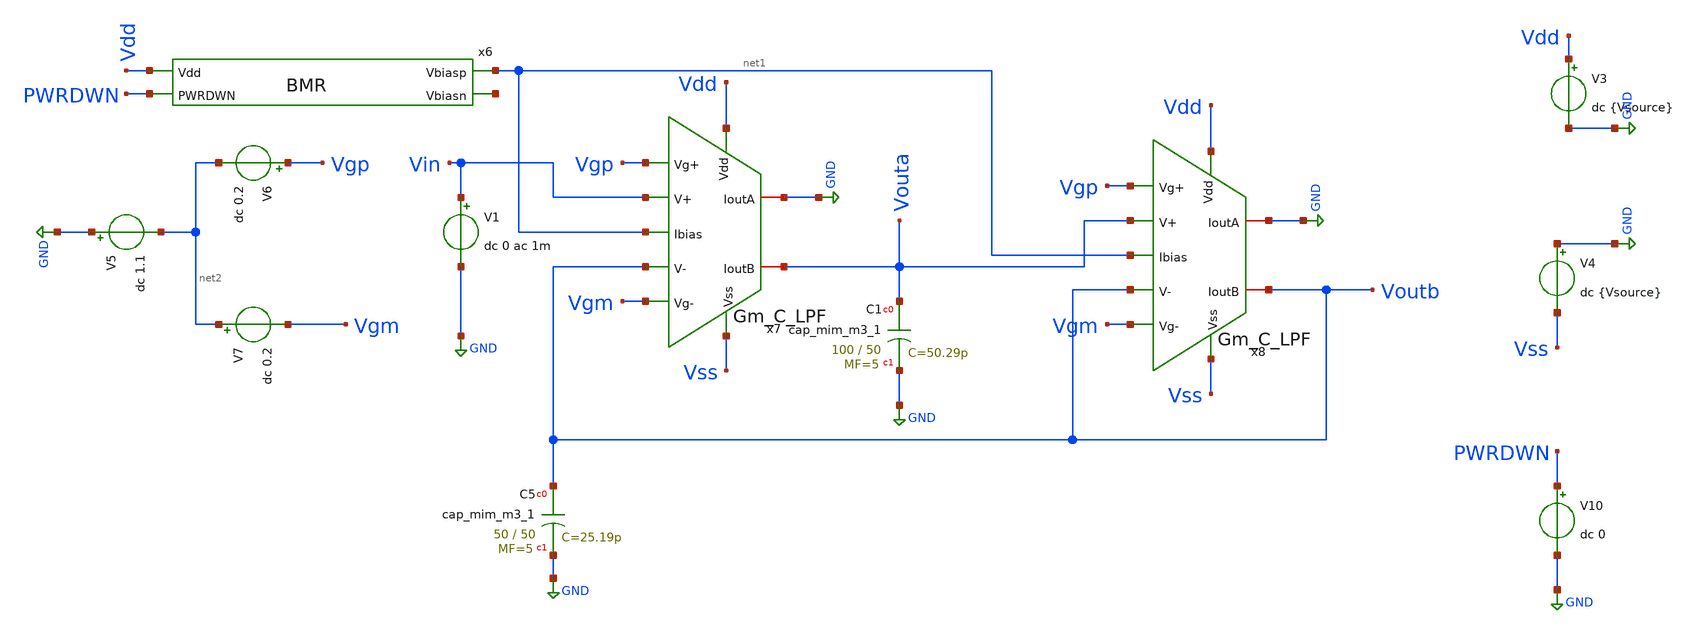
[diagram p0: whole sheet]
** sch_path: xschem/GmC_TB.sch
**.subckt GmC_TB
V4 GND Vss dc {Vsource}
V3 Vdd GND dc {Vsource}
V10 PWRDWN GND dc 0
V1 Vin GND dc 0 ac 1m
V5 GND net2 dc 1.1
V6 Vgp net2 dc 0.2
x6 Vdd net1 net3 PWRDWN BMR
x7 Vdd Vss Vgp Vgm GND Vouta Vin Voutb net1 Gm_C_LPF
V7 net2 Vgm dc 0.2
x8 Vdd Vss Vgp Vgm GND Voutb Vouta Voutb net1 Gm_C_LPF
XC5 Voutb GND sky130_fd_pr__cap_mim_m3_1 W=50 L=50 MF=5 m=5
XC1 Vouta GND sky130_fd_pr__cap_mim_m3_1 W=100 L=50 MF=5 m=5
**** begin user architecture code


.lib /foss/pdks/sky130A/libs.tech/combined/sky130.lib.spice ss_mm

***Centered at 40C and varies to a range of -20 to 100; with 20C being 1-standard dev***
.param TEMPGAUSS = agauss(40, 60, 3)

***Centered at 2.5V and varies to a range of 2V to 3V; with 0.16mV being 1-standard dev***
.param VOLTGAUSS = agauss(2.5, 0.5, 3)

.param ptemp = 'TEMPGAUSS'

.param Vsource = 'VOLTGAUSS'
.options temp = {ptemp}

.csparam ctemp = {ptemp}
.csparam cvolt = {Vsource}


.control
 let T = 27
 let V = 2.5

 let i_count = 100
 let T_vec = vector(i_count)
 let V_vec = vector(i_count)

 let CUTOFF_vec = vector(i_count)

 let index = 0

 set wr_vecnames
 dowhile index <= 100
   save all
   *tran 1u 2m
   *dc V1 -10m 10m 1m
   ac dec 100 0.1 1MEG

   write GMC_LPF_CUTOFFS_SS_MM_PVT.raw

   set noprintscale

   let gaindb = 'db(voutb/vin)'
   meas ac maxgain MAX gaindb
   let cutoffdb = 'maxgain - 3'
   meas ac cutoff_freq WHEN gaindb = cutoffdb
   let CUTOFF_vec[index] = 'cutoff_freq'

   **OFFSET**

   ***meas dc Off FIND v(voutb) WHEN v(vin) = 0 RISE = 1

   ***let OFFSET_vec[index] = 'Off'

   set appendwrite


   let V = $&cvolt
   let T = $&ctemp

   echo -n This is $&V
   echo -n This is $&T
   echo -n This is $&index

   let V_vec[index] = 'V'
   let T_vec[index] = 'T'

   let index = index + 1
   reset
 end
  **OL AC
  *** print col GAIN_vec UGW_vec PM_vec T_vec V_vec > FDA_AC_CM_GAIN_UGW_PM_SS_PVT.txt
  **Offset
   ***print col OFFSET_vec T_vec V_vec > GMC_LPF_OFFSETS_SS_MM_PVT.txt
    print col CUTOFF_vec T_vec V_vec > GMC_AC_CUTOFF_SS_MM_PVT.txt

.endc
.end

**** end user architecture code
**.ends

* expanding   symbol:  BMR.sym # of pins=4
** sym_path: xschem/BMR.sym
** sch_path: xschem/BMR.sch
.subckt BMR Vdd Vbiasp Vbiasn PWRDWN
*.ipin Vdd
*.opin Vbiasn
*.opin Vbiasp
*.ipin PWRDWN
XM3 Vbiasn Vbiasn GND GND sky130_fd_pr__nfet_g5v0d10v5 L=3 W=1.4 nf=1 ad='int((1 + 1)/2) * 1.4 / 1 * 0.29'
+ as='int((1 + 2)/2) * 1.4 / 1 * 0.29' pd='2*int((1 + 1)/2) * (1.4 / 1 + 0.29)' ps='2*int((1 + 2)/2) * (1.4 / 1 + 0.29)'
+ nrd='0.29 / 1.4 ' nrs='0.29 / 1.4 ' sa=0 sb=0 sd=0 mult=1 m=1
XM1 Vbiasp Vbiasp Vdd Vdd sky130_fd_pr__pfet_g5v0d10v5 L=3 W=31 nf=8 ad='int((8 + 1)/2) * 31 / 8 * 0.29'
+ as='int((8 + 2)/2) * 31 / 8 * 0.29' pd='2*int((8 + 1)/2) * (31 / 8 + 0.29)' ps='2*int((8 + 2)/2) * (31 / 8 + 0.29)'
+ nrd='0.29 / 31 ' nrs='0.29 / 31 ' sa=0 sb=0 sd=0 mult=2 m=2
XM2 Vbiasn Vbiasp Vdd Vdd sky130_fd_pr__pfet_g5v0d10v5 L=3 W=31 nf=8 ad='int((8 + 1)/2) * 31 / 8 * 0.29'
+ as='int((8 + 2)/2) * 31 / 8 * 0.29' pd='2*int((8 + 1)/2) * (31 / 8 + 0.29)' ps='2*int((8 + 2)/2) * (31 / 8 + 0.29)'
+ nrd='0.29 / 31 ' nrs='0.29 / 31 ' sa=0 sb=0 sd=0 mult=2 m=2
XM11 net1 PWRUP Vdd Vdd sky130_fd_pr__pfet_g5v0d10v5 L=10 W=1 nf=1 ad='int((1 + 1)/2) * 1 / 1 * 0.29'
+ as='int((1 + 2)/2) * 1 / 1 * 0.29' pd='2*int((1 + 1)/2) * (1 / 1 + 0.29)' ps='2*int((1 + 2)/2) * (1 / 1 + 0.29)'
+ nrd='0.29 / 1 ' nrs='0.29 / 1 ' sa=0 sb=0 sd=0 mult=1 m=1
XM4 Vbiasp Vbiasn net2 GND sky130_fd_pr__nfet_g5v0d10v5 L=3 W=1.4 nf=1 ad='int((1 + 1)/2) * 1.4 / 1 * 0.29'
+ as='int((1 + 2)/2) * 1.4 / 1 * 0.29' pd='2*int((1 + 1)/2) * (1.4 / 1 + 0.29)' ps='2*int((1 + 2)/2) * (1.4 / 1 + 0.29)'
+ nrd='0.29 / 1.4 ' nrs='0.29 / 1.4 ' sa=0 sb=0 sd=0 mult=2 m=2
XM5 net1 Vbiasn GND GND sky130_fd_pr__nfet_g5v0d10v5 L=3 W=1.4 nf=1 ad='int((1 + 1)/2) * 1.4 / 1 * 0.29'
+ as='int((1 + 2)/2) * 1.4 / 1 * 0.29' pd='2*int((1 + 1)/2) * (1.4 / 1 + 0.29)' ps='2*int((1 + 2)/2) * (1.4 / 1 + 0.29)'
+ nrd='0.29 / 1.4 ' nrs='0.29 / 1.4 ' sa=0 sb=0 sd=0 mult=1 m=1
XM7 net3 net1 Vbiasn GND sky130_fd_pr__nfet_g5v0d10v5 L=1 W=20 nf=1 ad='int((1 + 1)/2) * 20 / 1 * 0.29'
+ as='int((1 + 2)/2) * 20 / 1 * 0.29' pd='2*int((1 + 1)/2) * (20 / 1 + 0.29)' ps='2*int((1 + 2)/2) * (20 / 1 + 0.29)'
+ nrd='0.29 / 20 ' nrs='0.29 / 20 ' sa=0 sb=0 sd=0 mult=1 m=1
x1 Vdd PWRUP PWRDWN GND NOT_GATE
XM12 Vbiasp PWRUP net3 GND sky130_fd_pr__nfet_g5v0d10v5 L=1 W=20 nf=1 ad='int((1 + 1)/2) * 20 / 1 * 0.29'
+ as='int((1 + 2)/2) * 20 / 1 * 0.29' pd='2*int((1 + 1)/2) * (20 / 1 + 0.29)' ps='2*int((1 + 2)/2) * (20 / 1 + 0.29)'
+ nrd='0.29 / 20 ' nrs='0.29 / 20 ' sa=0 sb=0 sd=0 mult=1 m=1
XM9 Vbiasp PWRUP Vdd Vdd sky130_fd_pr__pfet_g5v0d10v5 L=1 W=3 nf=1 ad='int((1 + 1)/2) * 3 / 1 * 0.29'
+ as='int((1 + 2)/2) * 3 / 1 * 0.29' pd='2*int((1 + 1)/2) * (3 / 1 + 0.29)' ps='2*int((1 + 2)/2) * (3 / 1 + 0.29)'
+ nrd='0.29 / 3 ' nrs='0.29 / 3 ' sa=0 sb=0 sd=0 mult=1 m=1
XM10 Vbiasn PWRDWN GND GND sky130_fd_pr__nfet_g5v0d10v5 L=1 W=1 nf=1 ad='int((1 + 1)/2) * 1 / 1 * 0.29'
+ as='int((1 + 2)/2) * 1 / 1 * 0.29' pd='2*int((1 + 1)/2) * (1 / 1 + 0.29)' ps='2*int((1 + 2)/2) * (1 / 1 + 0.29)'
+ nrd='0.29 / 1 ' nrs='0.29 / 1 ' sa=0 sb=0 sd=0 mult=1 m=1
XR5 GND net2 GND sky130_fd_pr__res_xhigh_po_2p85 L=71.25 mult=1 m=1
XC10 Vdd net1 sky130_fd_pr__cap_mim_m3_1 W=10 L=10 MF=5 m=5
XC2 Vdd Vbiasp sky130_fd_pr__cap_mim_m3_1 W=10 L=10 MF=5 m=5
XC1 Vbiasn GND sky130_fd_pr__cap_mim_m3_1 W=10 L=10 MF=5 m=5
.ends


* expanding   symbol:  Gm_C_LPF.sym # of pins=9
** sym_path: xschem/Gm_C_LPF.sym
** sch_path: xschem/Gm_C_LPF.sch
.subckt Gm_C_LPF Vdd Vss Vg+ Vg- IoutA IoutB V+ V- Ibias
*.ipin V-
*.ipin V+
*.ipin Vdd
*.ipin Vss
*.ipin Ibias
*.ipin Vg-
*.ipin Vg+
*.iopin IoutA
*.iopin IoutB
XM1 net2 Ibias Vdd Vdd sky130_fd_pr__pfet_g5v0d10v5 L=3 W=31 nf=8 ad='int((8 + 1)/2) * 31 / 8 * 0.29'
+ as='int((8 + 2)/2) * 31 / 8 * 0.29' pd='2*int((8 + 1)/2) * (31 / 8 + 0.29)' ps='2*int((8 + 2)/2) * (31 / 8 + 0.29)'
+ nrd='0.29 / 31 ' nrs='0.29 / 31 ' sa=0 sb=0 sd=0 mult=1 m=1
XM2 net3 V- net2 Vdd sky130_fd_pr__pfet_g5v0d10v5 L=3 W=40 nf=4 ad='int((4 + 1)/2) * 40 / 4 * 0.29' as='int((4 + 2)/2) * 40 / 4 * 0.29'
+ pd='2*int((4 + 1)/2) * (40 / 4 + 0.29)' ps='2*int((4 + 2)/2) * (40 / 4 + 0.29)' nrd='0.29 / 40 ' nrs='0.29 / 40 '
+ sa=0 sb=0 sd=0 mult=4 m=4
XM3 net4 V+ net1 Vdd sky130_fd_pr__pfet_g5v0d10v5 L=3 W=40 nf=4 ad='int((4 + 1)/2) * 40 / 4 * 0.29' as='int((4 + 2)/2) * 40 / 4 * 0.29'
+ pd='2*int((4 + 1)/2) * (40 / 4 + 0.29)' ps='2*int((4 + 2)/2) * (40 / 4 + 0.29)' nrd='0.29 / 40 ' nrs='0.29 / 40 '
+ sa=0 sb=0 sd=0 mult=4 m=4
XM4 net6 net3 Vss Vss sky130_fd_pr__nfet_g5v0d10v5 L=6 W=1 nf=1 ad='int((1 + 1)/2) * 1 / 1 * 0.29' as='int((1 + 2)/2) * 1 / 1 * 0.29'
+ pd='2*int((1 + 1)/2) * (1 / 1 + 0.29)' ps='2*int((1 + 2)/2) * (1 / 1 + 0.29)' nrd='0.29 / 1 ' nrs='0.29 / 1 '
+ sa=0 sb=0 sd=0 mult=4 m=4
XM5 net7 net4 Vss Vss sky130_fd_pr__nfet_g5v0d10v5 L=6 W=1 nf=1 ad='int((1 + 1)/2) * 1 / 1 * 0.29' as='int((1 + 2)/2) * 1 / 1 * 0.29'
+ pd='2*int((1 + 1)/2) * (1 / 1 + 0.29)' ps='2*int((1 + 2)/2) * (1 / 1 + 0.29)' nrd='0.29 / 1 ' nrs='0.29 / 1 '
+ sa=0 sb=0 sd=0 mult=4 m=4
XM6 net9 net3 Vss Vss sky130_fd_pr__nfet_g5v0d10v5 L=6 W=1 nf=1 ad='int((1 + 1)/2) * 1 / 1 * 0.29' as='int((1 + 2)/2) * 1 / 1 * 0.29'
+ pd='2*int((1 + 1)/2) * (1 / 1 + 0.29)' ps='2*int((1 + 2)/2) * (1 / 1 + 0.29)' nrd='0.29 / 1 ' nrs='0.29 / 1 '
+ sa=0 sb=0 sd=0 mult=4 m=4
XM7 net10 net4 Vss Vss sky130_fd_pr__nfet_g5v0d10v5 L=6 W=1 nf=1 ad='int((1 + 1)/2) * 1 / 1 * 0.29' as='int((1 + 2)/2) * 1 / 1 * 0.29'
+ pd='2*int((1 + 1)/2) * (1 / 1 + 0.29)' ps='2*int((1 + 2)/2) * (1 / 1 + 0.29)' nrd='0.29 / 1 ' nrs='0.29 / 1 '
+ sa=0 sb=0 sd=0 mult=4 m=4
XM8 net5 net5 Vdd Vdd sky130_fd_pr__pfet_g5v0d10v5 L=3 W=40 nf=4 ad='int((4 + 1)/2) * 40 / 4 * 0.29'
+ as='int((4 + 2)/2) * 40 / 4 * 0.29' pd='2*int((4 + 1)/2) * (40 / 4 + 0.29)' ps='2*int((4 + 2)/2) * (40 / 4 + 0.29)'
+ nrd='0.29 / 40 ' nrs='0.29 / 40 ' sa=0 sb=0 sd=0 mult=4 m=4
XM9 IoutA net5 Vdd Vdd sky130_fd_pr__pfet_g5v0d10v5 L=3 W=40 nf=4 ad='int((4 + 1)/2) * 40 / 4 * 0.29'
+ as='int((4 + 2)/2) * 40 / 4 * 0.29' pd='2*int((4 + 1)/2) * (40 / 4 + 0.29)' ps='2*int((4 + 2)/2) * (40 / 4 + 0.29)'
+ nrd='0.29 / 40 ' nrs='0.29 / 40 ' sa=0 sb=0 sd=0 mult=4 m=4
XM10 net1 Ibias Vdd Vdd sky130_fd_pr__pfet_g5v0d10v5 L=3 W=31 nf=8 ad='int((8 + 1)/2) * 31 / 8 * 0.29'
+ as='int((8 + 2)/2) * 31 / 8 * 0.29' pd='2*int((8 + 1)/2) * (31 / 8 + 0.29)' ps='2*int((8 + 2)/2) * (31 / 8 + 0.29)'
+ nrd='0.29 / 31 ' nrs='0.29 / 31 ' sa=0 sb=0 sd=0 mult=1 m=1
XM11 net3 Vg+ net6 Vss sky130_fd_pr__nfet_g5v0d10v5 L=6 W=1 nf=1 ad='int((1 + 1)/2) * 1 / 1 * 0.29' as='int((1 + 2)/2) * 1 / 1 * 0.29'
+ pd='2*int((1 + 1)/2) * (1 / 1 + 0.29)' ps='2*int((1 + 2)/2) * (1 / 1 + 0.29)' nrd='0.29 / 1 ' nrs='0.29 / 1 '
+ sa=0 sb=0 sd=0 mult=2 m=2
XM12 net3 Vg- net6 Vss sky130_fd_pr__nfet_g5v0d10v5 L=6 W=1 nf=1 ad='int((1 + 1)/2) * 1 / 1 * 0.29' as='int((1 + 2)/2) * 1 / 1 * 0.29'
+ pd='2*int((1 + 1)/2) * (1 / 1 + 0.29)' ps='2*int((1 + 2)/2) * (1 / 1 + 0.29)' nrd='0.29 / 1 ' nrs='0.29 / 1 '
+ sa=0 sb=0 sd=0 mult=2 m=2
XM13 net4 Vg- net7 Vss sky130_fd_pr__nfet_g5v0d10v5 L=6 W=1 nf=1 ad='int((1 + 1)/2) * 1 / 1 * 0.29' as='int((1 + 2)/2) * 1 / 1 * 0.29'
+ pd='2*int((1 + 1)/2) * (1 / 1 + 0.29)' ps='2*int((1 + 2)/2) * (1 / 1 + 0.29)' nrd='0.29 / 1 ' nrs='0.29 / 1 '
+ sa=0 sb=0 sd=0 mult=2 m=2
XM14 net4 Vg+ net7 Vss sky130_fd_pr__nfet_g5v0d10v5 L=6 W=1 nf=1 ad='int((1 + 1)/2) * 1 / 1 * 0.29' as='int((1 + 2)/2) * 1 / 1 * 0.29'
+ pd='2*int((1 + 1)/2) * (1 / 1 + 0.29)' ps='2*int((1 + 2)/2) * (1 / 1 + 0.29)' nrd='0.29 / 1 ' nrs='0.29 / 1 '
+ sa=0 sb=0 sd=0 mult=2 m=2
XM16 net8 net8 Vdd Vdd sky130_fd_pr__pfet_g5v0d10v5 L=3 W=40 nf=4 ad='int((4 + 1)/2) * 40 / 4 * 0.29'
+ as='int((4 + 2)/2) * 40 / 4 * 0.29' pd='2*int((4 + 1)/2) * (40 / 4 + 0.29)' ps='2*int((4 + 2)/2) * (40 / 4 + 0.29)'
+ nrd='0.29 / 40 ' nrs='0.29 / 40 ' sa=0 sb=0 sd=0 mult=4 m=4
XM17 IoutB net8 Vdd Vdd sky130_fd_pr__pfet_g5v0d10v5 L=3 W=40 nf=4 ad='int((4 + 1)/2) * 40 / 4 * 0.29'
+ as='int((4 + 2)/2) * 40 / 4 * 0.29' pd='2*int((4 + 1)/2) * (40 / 4 + 0.29)' ps='2*int((4 + 2)/2) * (40 / 4 + 0.29)'
+ nrd='0.29 / 40 ' nrs='0.29 / 40 ' sa=0 sb=0 sd=0 mult=4 m=4
XM15 net8 Vg- net9 Vss sky130_fd_pr__nfet_g5v0d10v5 L=6 W=1 nf=1 ad='int((1 + 1)/2) * 1 / 1 * 0.29' as='int((1 + 2)/2) * 1 / 1 * 0.29'
+ pd='2*int((1 + 1)/2) * (1 / 1 + 0.29)' ps='2*int((1 + 2)/2) * (1 / 1 + 0.29)' nrd='0.29 / 1 ' nrs='0.29 / 1 '
+ sa=0 sb=0 sd=0 mult=2 m=2
XM18 net5 Vg+ net9 Vss sky130_fd_pr__nfet_g5v0d10v5 L=6 W=1 nf=1 ad='int((1 + 1)/2) * 1 / 1 * 0.29' as='int((1 + 2)/2) * 1 / 1 * 0.29'
+ pd='2*int((1 + 1)/2) * (1 / 1 + 0.29)' ps='2*int((1 + 2)/2) * (1 / 1 + 0.29)' nrd='0.29 / 1 ' nrs='0.29 / 1 '
+ sa=0 sb=0 sd=0 mult=2 m=2
XM19 IoutA Vg+ net10 Vss sky130_fd_pr__nfet_g5v0d10v5 L=6 W=1 nf=1 ad='int((1 + 1)/2) * 1 / 1 * 0.29'
+ as='int((1 + 2)/2) * 1 / 1 * 0.29' pd='2*int((1 + 1)/2) * (1 / 1 + 0.29)' ps='2*int((1 + 2)/2) * (1 / 1 + 0.29)'
+ nrd='0.29 / 1 ' nrs='0.29 / 1 ' sa=0 sb=0 sd=0 mult=2 m=2
XM20 IoutB Vg- net10 Vss sky130_fd_pr__nfet_g5v0d10v5 L=6 W=1 nf=1 ad='int((1 + 1)/2) * 1 / 1 * 0.29'
+ as='int((1 + 2)/2) * 1 / 1 * 0.29' pd='2*int((1 + 1)/2) * (1 / 1 + 0.29)' ps='2*int((1 + 2)/2) * (1 / 1 + 0.29)'
+ nrd='0.29 / 1 ' nrs='0.29 / 1 ' sa=0 sb=0 sd=0 mult=2 m=2
XM21 net1 V- net2 Vdd sky130_fd_pr__pfet_g5v0d10v5 L=3 W=24 nf=4 ad='int((4 + 1)/2) * 24 / 4 * 0.29'
+ as='int((4 + 2)/2) * 24 / 4 * 0.29' pd='2*int((4 + 1)/2) * (24 / 4 + 0.29)' ps='2*int((4 + 2)/2) * (24 / 4 + 0.29)'
+ nrd='0.29 / 24 ' nrs='0.29 / 24 ' sa=0 sb=0 sd=0 mult=1 m=1
XM22 net2 V+ net1 Vdd sky130_fd_pr__pfet_g5v0d10v5 L=3 W=24 nf=4 ad='int((4 + 1)/2) * 24 / 4 * 0.29'
+ as='int((4 + 2)/2) * 24 / 4 * 0.29' pd='2*int((4 + 1)/2) * (24 / 4 + 0.29)' ps='2*int((4 + 2)/2) * (24 / 4 + 0.29)'
+ nrd='0.29 / 24 ' nrs='0.29 / 24 ' sa=0 sb=0 sd=0 mult=1 m=1
.ends


* expanding   symbol:  NOT_GATE.sym # of pins=4
** sym_path: xschem/NOT_GATE.sym
** sch_path: xschem/NOT_GATE.sch
.subckt NOT_GATE Vdd Vout Vin Vss
*.opin Vout
*.ipin Vdd
*.ipin Vss
*.ipin Vin
XM1 Vout Vin Vss Vss sky130_fd_pr__nfet_g5v0d10v5 L=1 W=1 nf=1 ad='int((1 + 1)/2) * 1 / 1 * 0.29' as='int((1 + 2)/2) * 1 / 1 * 0.29'
+ pd='2*int((1 + 1)/2) * (1 / 1 + 0.29)' ps='2*int((1 + 2)/2) * (1 / 1 + 0.29)' nrd='0.29 / 1 ' nrs='0.29 / 1 '
+ sa=0 sb=0 sd=0 mult=1 m=1
XM2 Vout Vin Vdd Vdd sky130_fd_pr__pfet_g5v0d10v5 L=1 W=3 nf=1 ad='int((1 + 1)/2) * 3 / 1 * 0.29' as='int((1 + 2)/2) * 3 / 1 * 0.29'
+ pd='2*int((1 + 1)/2) * (3 / 1 + 0.29)' ps='2*int((1 + 2)/2) * (3 / 1 + 0.29)' nrd='0.29 / 3 ' nrs='0.29 / 3 '
+ sa=0 sb=0 sd=0 mult=1 m=1
.ends

.GLOBAL GND
.end
